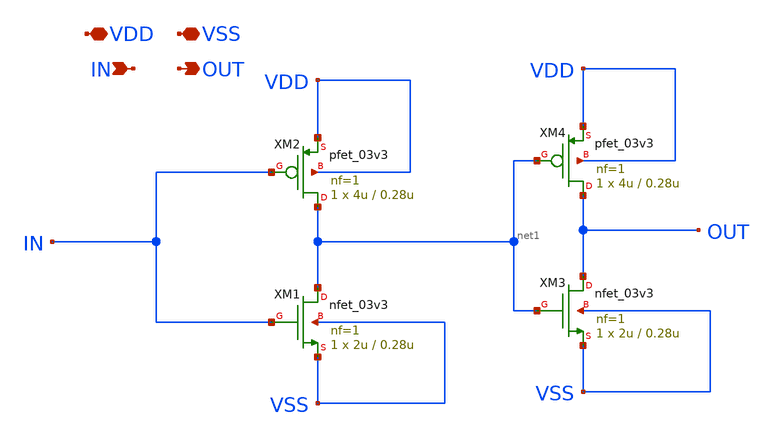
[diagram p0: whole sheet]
** sch_path: Clock_Generator_PAKISTAN_02/Schematics/buffer_loading.sch
**.subckt buffer_loading VDD VSS IN OUT
*.iopin VDD
*.iopin VSS
*.ipin IN
*.opin OUT
XM1 net1 IN VSS VSS nfet_03v3 L=0.28u W=2u nf=1 ad='int((nf+1)/2) * W/nf * 0.18u' as='int((nf+2)/2) * W/nf * 0.18u'
+ pd='2*int((nf+1)/2) * (W/nf + 0.18u)' ps='2*int((nf+2)/2) * (W/nf + 0.18u)' nrd='0.18u / W' nrs='0.18u / W'
+ sa=0 sb=0 sd=0 m=1
XM2 net1 IN VDD VDD pfet_03v3 L=0.28u W=4u nf=1 ad='int((nf+1)/2) * W/nf * 0.18u' as='int((nf+2)/2) * W/nf * 0.18u'
+ pd='2*int((nf+1)/2) * (W/nf + 0.18u)' ps='2*int((nf+2)/2) * (W/nf + 0.18u)' nrd='0.18u / W' nrs='0.18u / W'
+ sa=0 sb=0 sd=0 m=1
XM3 OUT net1 VSS VSS nfet_03v3 L=0.28u W=2u nf=1 ad='int((nf+1)/2) * W/nf * 0.18u' as='int((nf+2)/2) * W/nf * 0.18u'
+ pd='2*int((nf+1)/2) * (W/nf + 0.18u)' ps='2*int((nf+2)/2) * (W/nf + 0.18u)' nrd='0.18u / W' nrs='0.18u / W'
+ sa=0 sb=0 sd=0 m=1
XM4 OUT net1 VDD VDD pfet_03v3 L=0.28u W=4u nf=1 ad='int((nf+1)/2) * W/nf * 0.18u' as='int((nf+2)/2) * W/nf * 0.18u'
+ pd='2*int((nf+1)/2) * (W/nf + 0.18u)' ps='2*int((nf+2)/2) * (W/nf + 0.18u)' nrd='0.18u / W' nrs='0.18u / W'
+ sa=0 sb=0 sd=0 m=1
**.ends
.end
